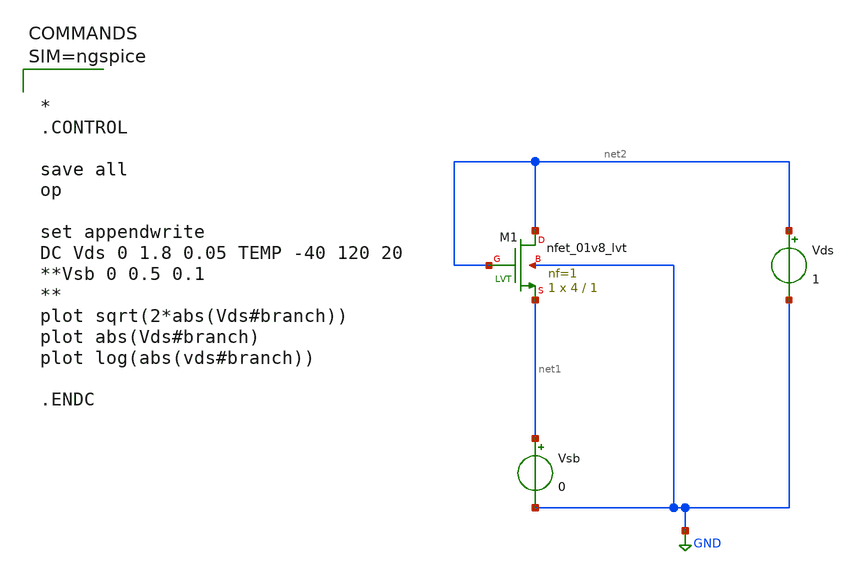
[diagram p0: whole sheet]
** sch_path: work/xschem/nmos_1.sch
**.subckt nmos_1
XM1 net2 net2 net1 GND sky130_fd_pr__nfet_01v8_lvt L=1 W=4 nf=1 ad='int((1 + 1)/2) * 4 / 1 * 0.29' as='int((1 + 2)/2) * 4 / 1 * 0.29'
+ pd='2*int((1 + 1)/2) * (4 / 1 + 0.29)' ps='2*int((1 + 2)/2) * (4 / 1 + 0.29)' nrd='0.29 / 4 ' nrs='0.29 / 4 '
+ sa=0 sb=0 sd=0 mult=1 m=1
Vsb net1 GND 0
Vds net2 GND 1
**** begin user architecture code



*
.CONTROL

save all
op

set appendwrite
DC Vds 0 1.8 0.05 TEMP -40 120 20
**Vsb 0 0.5 0.1
**
plot sqrt(2*abs(Vds#branch))
plot abs(Vds#branch)
plot log(abs(vds#branch))

.ENDC




** opencircuitdesign pdks install
.lib $::SKYWATER_MODELS/sky130.lib.spice tt

**** end user architecture code
**.ends
.GLOBAL GND
.end
